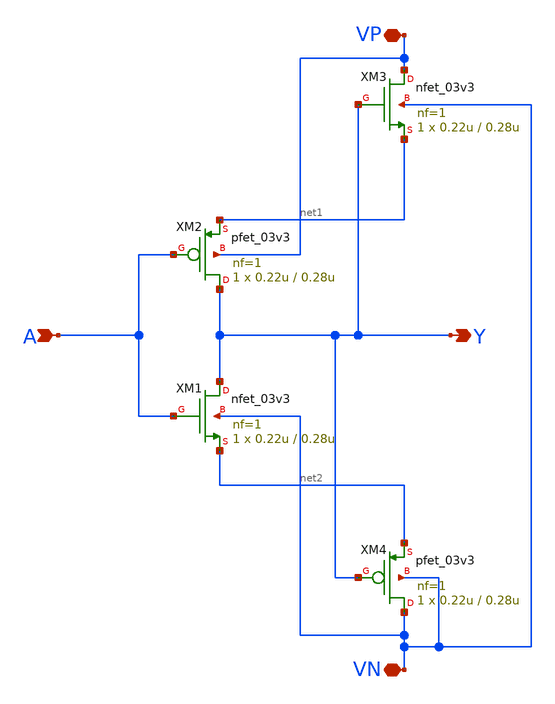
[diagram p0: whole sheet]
** sch_path: dls_inverter.sch
**.subckt dls_inverter A VN VP Y
*.ipin A
*.iopin VN
*.iopin VP
*.opin Y
XM1 Y A net2 VN nfet_03v3 L=0.28u W=0.22u nf=1 ad='int((nf+1)/2) * W/nf * 0.18u' as='int((nf+2)/2) * W/nf * 0.18u'
+ pd='2*int((nf+1)/2) * (W/nf + 0.18u)' ps='2*int((nf+2)/2) * (W/nf + 0.18u)' nrd='0.18u / W' nrs='0.18u / W'
+ sa=0 sb=0 sd=0 m=1 par=1
XM2 Y A net1 VP pfet_03v3 L=0.28u W=0.22u nf=1 ad='int((nf+1)/2) * W/nf * 0.18u' as='int((nf+2)/2) * W/nf * 0.18u'
+ pd='2*int((nf+1)/2) * (W/nf + 0.18u)' ps='2*int((nf+2)/2) * (W/nf + 0.18u)' nrd='0.18u / W' nrs='0.18u / W'
+ sa=0 sb=0 sd=0 m=1 par=1
XM3 VP Y net1 VN nfet_03v3 L=0.28u W=0.22u nf=1 ad='int((nf+1)/2) * W/nf * 0.18u' as='int((nf+2)/2) * W/nf * 0.18u'
+ pd='2*int((nf+1)/2) * (W/nf + 0.18u)' ps='2*int((nf+2)/2) * (W/nf + 0.18u)' nrd='0.18u / W' nrs='0.18u / W'
+ sa=0 sb=0 sd=0 m=1 par=1
XM4 VN Y net2 VN pfet_03v3 L=0.28u W=0.22u nf=1 ad='int((nf+1)/2) * W/nf * 0.18u' as='int((nf+2)/2) * W/nf * 0.18u'
+ pd='2*int((nf+1)/2) * (W/nf + 0.18u)' ps='2*int((nf+2)/2) * (W/nf + 0.18u)' nrd='0.18u / W' nrs='0.18u / W'
+ sa=0 sb=0 sd=0 m=1 par=1
**.ends
.end
